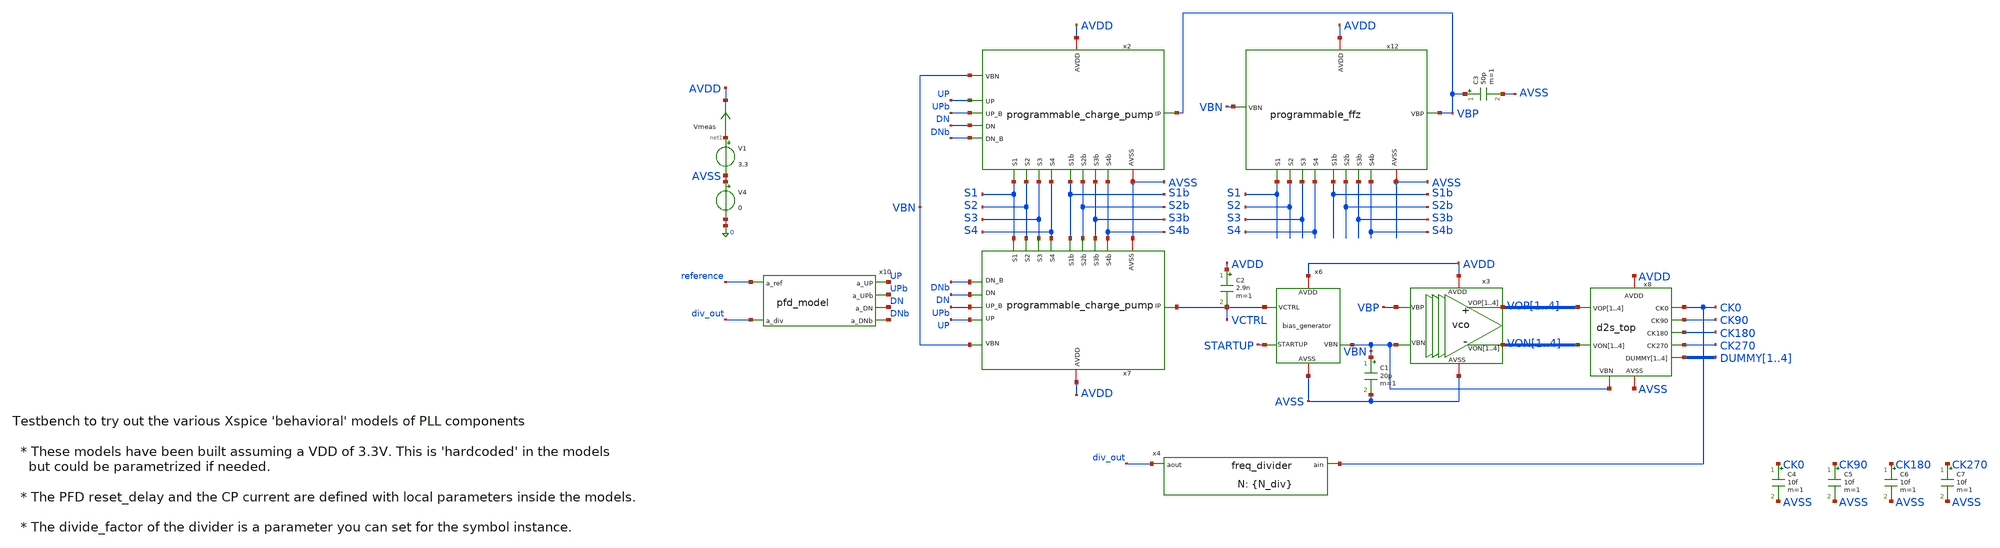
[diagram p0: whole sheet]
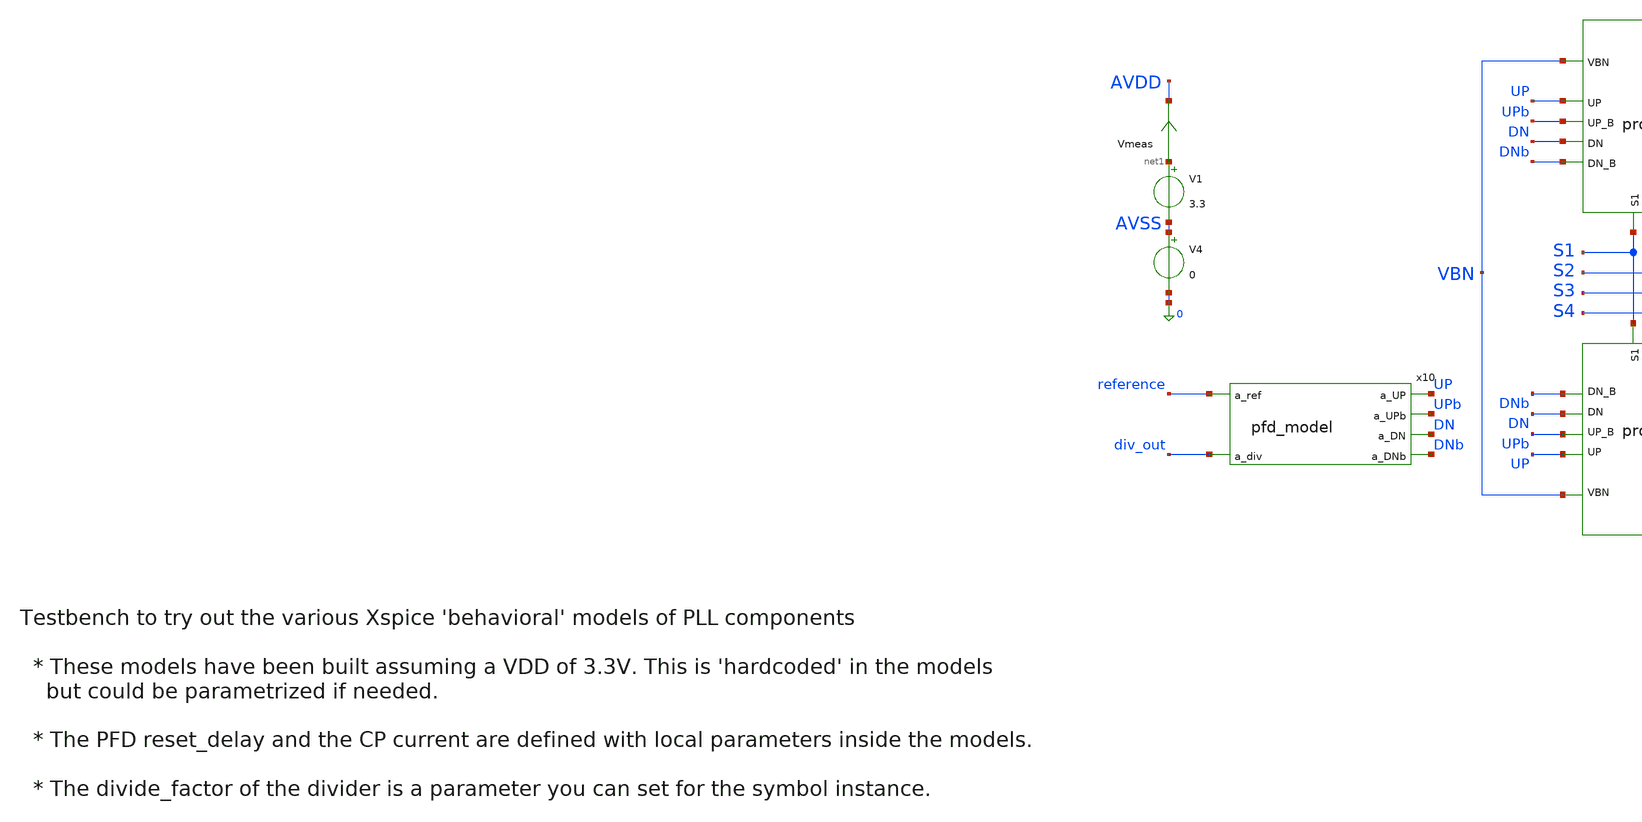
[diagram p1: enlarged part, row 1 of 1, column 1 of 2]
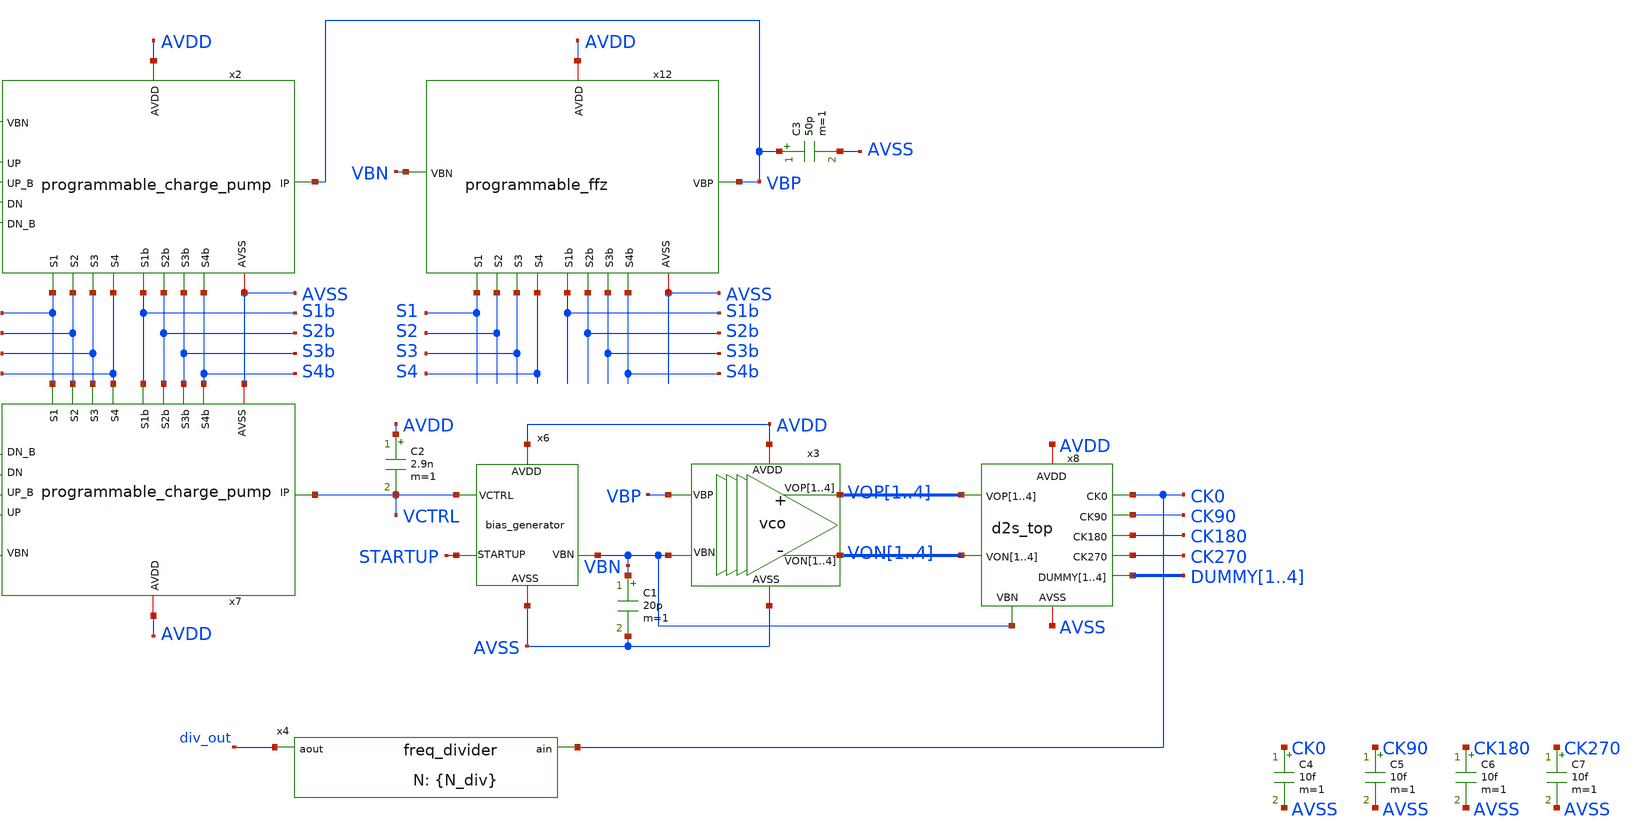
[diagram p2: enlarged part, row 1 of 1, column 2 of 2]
** sch_path: designs/libs/tb_pll/tb_PLL_CP_VCO_model.sch
**.subckt tb_PLL_CP_VCO_model
x4 div_out CK0 freq_divider divide_factor={N_div}
x3 VOP1 VOP2 VOP3 VOP4 VON1 VON2 VON3 VON4 AVDD AVSS VBP VBN vco
x6 VCTRL AVDD STARTUP AVSS VBN bias_generator
C2 AVDD VCTRL 2.9n m=1
V1 net1 AVSS 3.3
V4 AVSS 0 0
x2 AVSS AVDD UP UPb DN VBP DNb VBN S1b S1 S2b S2 S3b S3 S4b S4 programmable_charge_pump
x7 AVSS AVDD UP UPb DN VCTRL DNb VBN S1b S1 S2b S2 S3b S3 S4b S4 programmable_charge_pump
C1 VBN AVSS 20p m=1
C3 VBP AVSS 50p m=1
x12 VBP AVSS AVDD VBN S1b S1 S2b S2 S3b S3 S4b S4 programmable_ffz
x8 VOP1 VOP2 VOP3 VOP4 VON1 VON2 VON3 VON4 VBN DUMMY1 DUMMY2 DUMMY3 DUMMY4 CK0 CK90 CK180 CK270 AVDD
+ AVSS d2s_top
C4 CK0 AVSS 10f m=1
C5 CK90 AVSS 10f m=1
C6 CK180 AVSS 10f m=1
C7 CK270 AVSS 10f m=1
x10 reference UP UPb DN div_out DNb pfd_model
Vmeas net1 AVDD 0
.save i(vmeas)
**** begin user architecture code

.include $::180MCU_MODELS/design.ngspice
.lib $::180MCU_MODELS/sm141064.ngspice typical
*.lib $::180MCU_MODELS/sm141064.ngspice SS
*.lib $::180MCU_MODELS/sm141064.ngspice FF
*.lib $::180MCU_MODELS/sm141064.ngspice SF
*.lib $::180MCU_MODELS/sm141064.ngspice FS



==============Fref, N======================
.param f_ref=10MEG N_div=30

.param d1=0 d2=3.3 d3=3.3 d4=3.3
.param d1b=3.3 d2b=0 d3b=0 d4b=0

.ic v(VCTRL)=1 v(vbp)=1
==============Frequency Calculation========
.param tp_ref='td_ref/2' td_ref='1/f_ref'
Vref reference gnd pulse(0 3.3 0 500p 500p tp_ref td_ref)

.ic v(vop1)=3.3 v(von1)=0 v(startup)=0
.options reltol=1e-5 cshunt=1e-15
.options method=gear

VS1 S1 0 d1
VS2 S2 0 d2
VS3 S3 0 d3
VS4 S4 0 d4

VS1b S1b 0 d1b
VS2b S2b 0 d2b
VS3b S3b 0 d3b
VS4b S4b 0 d4b

.control
set wr_singlescale
set wr_vecnames

save v(VCTRL) v(vbp) v(vbn) v(reference) v(div_out) v(pre_div) v(CK0) v(CK90) v(CK180) v(CK270)
+ v(up) v(dn)

tran 10p 180u

linearize v(CK0) v(CK90) v(CK180) v(CK270) v(VCTRL) v(up) v(dn) v(vbp) v(vbn) v(reference)
+ v(div_out) v(pre_div) i(vmeas)

remzerovec

write tb5_3.raw
wrdata /foss/designs/synchronos-chipathon-2026/designs/libs/scripts/sim_data/tb5_3.txt tran.all
destroy all
.endc


**** end user architecture code
**.ends

* expanding   symbol:  libs/model_pll/freq_divider.sym # of pins=2
** sym_path: libs/model_pll/freq_divider.sym
** sch_path: libs/model_pll/freq_divider.sch
.subckt freq_divider aout ain  divide_factor=20
*.ipin ain
*.opin aout
* noconn ain
* noconn aout
**** begin user architecture code


* Behavioral Frequency Divider with robust Mixed-Signal Bridges

* Top-level parameter (Defaults to 10 if not passed by symbol)
.param divide_factor = 10

* MATH FIX: Guarantees at least 1 high cycle, targets 50% duty cycle
.param high_cycles = {max(1, floor(divide_factor/2))}

* Xspice digital frequency divider
adiv din dout divider
.model divider d_fdiv(div_factor = {divide_factor}  high_cycles = {high_cycles}  i_count = 0  rise_delay
+ = 100p fall_delay = 100p )
*+ rise_delay = 500p fall_delay = 500p )

* WINDOW FIX: Widened analog-to-digital thresholds to catch fast sine waves
aADC [ ain ] [ din ] adc_buff
.model adc_buff adc_bridge(in_low = 1.2 in_high = 2.1 rise_delay = 10p fall_delay = 10p)

* Digital-to-analog bridge
aDAC [ dout ] [ aout ] dac_buff
.model dac_buff dac_bridge(out_low = 0 out_high = 3.3 t_rise = 500p t_fall = 500p)


**** end user architecture code
.ends


* expanding   symbol:  libs/core_analog/vco/vco.sym # of pins=6
** sym_path: designs/libs/core_analog/vco/vco.sym
** sch_path: designs/libs/core_analog/vco/vco.sch
.subckt vco VOP1 VOP2 VOP3 VOP4 VON1 VON2 VON3 VON4 AVDD AVSS VBP VBN
*.opin VOP1,VOP2,VOP3,VOP4
*.opin VON1,VON2,VON3,VON4
*.ipin VBP
*.ipin VBN
*.iopin AVDD
*.iopin AVSS
x1 VOP1 AVDD VOP4 VON4 VON1 AVSS VBP VBN delay_stage
x2 VOP2 AVDD VON1 VOP1 VON2 AVSS VBP VBN delay_stage
x3 VOP3 AVDD VON2 VOP2 VON3 AVSS VBP VBN delay_stage
x4 VOP4 AVDD VON3 VOP3 VON4 AVSS VBP VBN delay_stage
.ends


* expanding   symbol:  libs/core_analog/bias_generator/bias_generator.sym # of pins=5
** sym_path: designs/libs/core_analog/bias_generator/bias_generator.sym
** sch_path: designs/libs/core_analog/bias_generator/bias_generator.sch
.subckt bias_generator VCTRL AVDD STARTUP AVSS VBN
*.ipin VCTRL
*.ipin STARTUP
*.iopin AVDD
*.iopin AVSS
*.opin VBN
x1 VBN AVDD net2 VCTRL AVSS net1 ota_5t
XM1 net1 net1 AVDD AVDD pfet_03v3 L=0.5u W=16.8u nf=1 ad='int((nf+1)/2) * W/nf * 0.18u' as='int((nf+2)/2) * W/nf * 0.18u'
+ pd='2*int((nf+1)/2) * (W/nf + 0.18u)' ps='2*int((nf+2)/2) * (W/nf + 0.18u)' nrd='0.18u / W' nrs='0.18u / W'
+ sa=0 sb=0 sd=0 m=16
XM8 net2 AVDD net4 AVSS nfet_03v3 L=0.5u W=2.08u nf=1 ad='int((nf+1)/2) * W/nf * 0.18u' as='int((nf+2)/2) * W/nf * 0.18u'
+ pd='2*int((nf+1)/2) * (W/nf + 0.18u)' ps='2*int((nf+2)/2) * (W/nf + 0.18u)' nrd='0.18u / W' nrs='0.18u / W'
+ sa=0 sb=0 sd=0 m=8
XM11 net1 AVDD net3 AVSS nfet_03v3 L=0.5u W=2.08u nf=1 ad='int((nf+1)/2) * W/nf * 0.18u' as='int((nf+2)/2) * W/nf * 0.18u'
+ pd='2*int((nf+1)/2) * (W/nf + 0.18u)' ps='2*int((nf+2)/2) * (W/nf + 0.18u)' nrd='0.18u / W' nrs='0.18u / W'
+ sa=0 sb=0 sd=0 m=8
XM2 net2 VCTRL AVDD AVDD pfet_03v3 L=1.5u W=1.1u nf=1 ad='int((nf+1)/2) * W/nf * 0.18u' as='int((nf+2)/2) * W/nf * 0.18u'
+ pd='2*int((nf+1)/2) * (W/nf + 0.18u)' ps='2*int((nf+2)/2) * (W/nf + 0.18u)' nrd='0.18u / W' nrs='0.18u / W'
+ sa=0 sb=0 sd=0 m=8
XM5 net2 net2 AVDD AVDD pfet_03v3 L=1.5u W=1.1u nf=1 ad='int((nf+1)/2) * W/nf * 0.18u' as='int((nf+2)/2) * W/nf * 0.18u'
+ pd='2*int((nf+1)/2) * (W/nf + 0.18u)' ps='2*int((nf+2)/2) * (W/nf + 0.18u)' nrd='0.18u / W' nrs='0.18u / W'
+ sa=0 sb=0 sd=0 m=8
XM7 net4 VBN AVSS AVSS nfet_03v3 L=0.5u W=11.25u nf=1 ad='int((nf+1)/2) * W/nf * 0.18u' as='int((nf+2)/2) * W/nf * 0.18u'
+ pd='2*int((nf+1)/2) * (W/nf + 0.18u)' ps='2*int((nf+2)/2) * (W/nf + 0.18u)' nrd='0.18u / W' nrs='0.18u / W'
+ sa=0 sb=0 sd=0 m=8
XM3 net3 VBN AVSS AVSS nfet_03v3 L=0.5u W=11.25u nf=1 ad='int((nf+1)/2) * W/nf * 0.18u' as='int((nf+2)/2) * W/nf * 0.18u'
+ pd='2*int((nf+1)/2) * (W/nf + 0.18u)' ps='2*int((nf+2)/2) * (W/nf + 0.18u)' nrd='0.18u / W' nrs='0.18u / W'
+ sa=0 sb=0 sd=0 m=8
XM4 net3 STARTUP AVSS AVSS nfet_03v3 L=0.5u W=11.25u nf=1 ad='int((nf+1)/2) * W/nf * 0.18u' as='int((nf+2)/2) * W/nf * 0.18u'
+ pd='2*int((nf+1)/2) * (W/nf + 0.18u)' ps='2*int((nf+2)/2) * (W/nf + 0.18u)' nrd='0.18u / W' nrs='0.18u / W'
+ sa=0 sb=0 sd=0 m=2
.ends


* expanding   symbol:  libs/core_analog/programmable_charge_pump/programmable_charge_pump.sym # of
*+ pins=16
** sym_path: designs/libs/core_analog/programmable_charge_pump/programmable_charge_pump.sym
** sch_path: designs/libs/core_analog/programmable_charge_pump/programmable_charge_pump.sch
.subckt programmable_charge_pump AVSS AVDD UP UP_B DN IP DN_B VBN S1b S1 S2b S2 S3b S3 S4b S4
*.ipin VBN
*.ipin S1b
*.ipin S1
*.ipin S2b
*.ipin S2
*.ipin S3b
*.ipin S3
*.ipin S4b
*.ipin S4
*.iopin AVSS
*.iopin AVDD
*.ipin UP
*.ipin UP_B
*.ipin DN
*.ipin DN_B
*.opin IP
x1 AVDD AVSS UP UP_B DN DN_B VBN1 IP S1b charge_pump
x61 AVDD AVSS UP UP_B DN DN_B VBN2 IP S2b charge_pump
x62 AVDD AVSS UP UP_B DN DN_B VBN2 IP S2b charge_pump
x71 AVDD AVSS UP UP_B DN DN_B VBN3 IP S3b charge_pump
x72 AVDD AVSS UP UP_B DN DN_B VBN3 IP S3b charge_pump
x73 AVDD AVSS UP UP_B DN DN_B VBN3 IP S3b charge_pump
x74 AVDD AVSS UP UP_B DN DN_B VBN3 IP S3b charge_pump
x81 AVDD AVSS UP UP_B DN DN_B VBN4 IP S4b charge_pump
x82 AVDD AVSS UP UP_B DN DN_B VBN4 IP S4b charge_pump
x83 AVDD AVSS UP UP_B DN DN_B VBN4 IP S4b charge_pump
x84 AVDD AVSS UP UP_B DN DN_B VBN4 IP S4b charge_pump
x85 AVDD AVSS UP UP_B DN DN_B VBN4 IP S4b charge_pump
x86 AVDD AVSS UP UP_B DN DN_B VBN4 IP S4b charge_pump
x87 AVDD AVSS UP UP_B DN DN_B VBN4 IP S4b charge_pump
x88 AVDD AVSS UP UP_B DN DN_B VBN4 IP S4b charge_pump
x2 VBN AVSS S1 VBN1 S1b AVDD transmission_gate
x0 AVDD AVSS UP UP_B DN DN_B VBN IP AVSS charge_pump
x3 VBN AVSS S2 VBN2 S2b AVDD transmission_gate
x4 VBN AVSS S3 VBN3 S3b AVDD transmission_gate
x5 VBN AVSS S4 VBN4 S4b AVDD transmission_gate
.ends


* expanding   symbol:  libs/core_analog/programmable_ffz/programmable_ffz.sym # of pins=12
** sym_path: designs/libs/core_analog/programmable_ffz/programmable_ffz.sym
** sch_path: designs/libs/core_analog/programmable_ffz/programmable_ffz.sch
.subckt programmable_ffz VBP AVSS AVDD VBN S1b S1 S2b S2 S3b S3 S4b S4
*.ipin VBN
*.ipin S1b
*.ipin S1
*.ipin S2b
*.ipin S2
*.ipin S3b
*.ipin S3
*.ipin S4b
*.ipin S4
*.iopin AVSS
*.iopin AVDD
*.opin VBP
x2 VBN AVSS S1 VBN1 S1b AVDD transmission_gate
x3 VBN AVSS S2 VBN2 S2b AVDD transmission_gate
x4 VBN AVSS S3 VBN3 S3b AVDD transmission_gate
x5 VBN AVSS S4 VBN4 S4b AVDD transmission_gate
x1 AVDD VBP VBN AVSS AVSS feed_forward_zero
x6 AVDD net1 VBN1 S1b AVSS feed_forward_zero
x71 AVDD net2[1] VBN2 S2b AVSS feed_forward_zero
x72 AVDD net2[0] VBN2 S2b AVSS feed_forward_zero
x11 AVDD net3[3] VBN3 S3b AVSS feed_forward_zero
x12 AVDD net3[2] VBN3 S3b AVSS feed_forward_zero
x13 AVDD net3[1] VBN3 S3b AVSS feed_forward_zero
x14 AVDD net3[0] VBN3 S3b AVSS feed_forward_zero
x21 AVDD net4[7] VBN4 S4b AVSS feed_forward_zero
x22 AVDD net4[6] VBN4 S4b AVSS feed_forward_zero
x23 AVDD net4[5] VBN4 S4b AVSS feed_forward_zero
x24 AVDD net4[4] VBN4 S4b AVSS feed_forward_zero
x25 AVDD net4[3] VBN4 S4b AVSS feed_forward_zero
x26 AVDD net4[2] VBN4 S4b AVSS feed_forward_zero
x27 AVDD net4[1] VBN4 S4b AVSS feed_forward_zero
x28 AVDD net4[0] VBN4 S4b AVSS feed_forward_zero
x7 net1 AVSS S1 VBP S1b AVDD transmission_gate
x81 net2[1] AVSS S2 VBP S2b AVDD transmission_gate
x82 net2[0] AVSS S2 VBP S2b AVDD transmission_gate
x91 net3[3] AVSS S3 VBP S3b AVDD transmission_gate
x92 net3[2] AVSS S3 VBP S3b AVDD transmission_gate
x93 net3[1] AVSS S3 VBP S3b AVDD transmission_gate
x94 net3[0] AVSS S3 VBP S3b AVDD transmission_gate
x101 net4[7] AVSS S4 VBP S4b AVDD transmission_gate
x102 net4[6] AVSS S4 VBP S4b AVDD transmission_gate
x103 net4[5] AVSS S4 VBP S4b AVDD transmission_gate
x104 net4[4] AVSS S4 VBP S4b AVDD transmission_gate
x105 net4[3] AVSS S4 VBP S4b AVDD transmission_gate
x106 net4[2] AVSS S4 VBP S4b AVDD transmission_gate
x107 net4[1] AVSS S4 VBP S4b AVDD transmission_gate
x108 net4[0] AVSS S4 VBP S4b AVDD transmission_gate
.ends


* expanding   symbol:  libs/core_analog/d2s_top/d2s_top.sym # of pins=10
** sym_path: designs/libs/core_analog/d2s_top/d2s_top.sym
** sch_path: designs/libs/core_analog/d2s_top/d2s_top.sch
.subckt d2s_top VOP1 VOP2 VOP3 VOP4 VON1 VON2 VON3 VON4 VBN DUMMY1 DUMMY2 DUMMY3 DUMMY4 CK0 CK90
+ CK180 CK270 AVDD AVSS
*.ipin VOP1,VOP2,VOP3,VOP4
*.ipin VON1,VON2,VON3,VON4
*.ipin VBN
*.opin DUMMY1,DUMMY2,DUMMY3,DUMMY4
*.opin CK0
*.opin CK90
*.opin CK180
*.opin CK270
*.iopin AVDD
*.iopin AVSS
x1 AVDD AVSS VON1 VOP1 VBN net8 d2s_converter
x2 AVDD AVSS VON3 VOP3 VBN net1 d2s_converter
x9 AVDD net8 CK0 AVSS inv
x10 AVDD net1 CK90 AVSS inv
x3 AVDD AVSS VOP1 VON1 VBN net2 d2s_converter
x4 AVDD net2 CK180 AVSS inv
x5 AVDD AVSS VOP3 VON3 VBN net3 d2s_converter
x6 AVDD net3 CK270 AVSS inv
x7 AVDD AVSS VON2 VOP2 VBN net7 d2s_converter
x8 AVDD AVSS VON4 VOP4 VBN net4 d2s_converter
x11 AVDD net7 DUMMY1 AVSS inv
x12 AVDD net4 DUMMY2 AVSS inv
x13 AVDD AVSS VOP2 VON2 VBN net5 d2s_converter
x14 AVDD net5 DUMMY3 AVSS inv
x15 AVDD AVSS VOP4 VON4 VBN net6 d2s_converter
x16 AVDD net6 DUMMY4 AVSS inv
.ends


* expanding   symbol:  libs/model_pll/pfd_model.sym # of pins=6
** sym_path: designs/libs/model_pll/pfd_model.sym
** sch_path: designs/libs/model_pll/pfd_model.sch
.subckt pfd_model a_ref a_UP a_UPb a_DN a_div a_DNb
*.ipin a_ref
*.ipin a_div
*.opin a_UP
*.opin a_UPb
*.opin a_DN
*.opin a_DNb
* noconn a_ref
* noconn a_div
* noconn a_UP
* noconn a_UPb
* noconn a_DN
* noconn a_DNb
**** begin user architecture code


* PFD Model using digital Xspice components

* pfd_delay local parameter sets the duration of the overlap (dead-band elimination)
* Reduced from 10ns to 200ps to prevent massive Vctrl ripple
*.param pfd_delay = 200p
.param pfd_delay = 2n
*.param pfd_delay = 10n

** Digital 1 and 0 to drive Flip-Flops
aone 0 d_d1 d_inv
azero d_d1 d_d0 d_inv
.model d_inv d_inverter()

** Flip Flops
ad1 d_d1 d_R d_d0 d_rset d_U d_U_ flop1
ad2 d_d1 d_V d_d0 d_rset d_D d_D_ flop1
.model flop1 d_dff(clk_delay = 1.0e-10 set_delay = 1.0e-10  reset_delay = {pfd_delay} ic = 2 rise_delay
+ = 1.0e-10  fall_delay = 1e-10)

* AND Gate
aa1 [d_U d_D] d_rset and1
.model and1 d_and(rise_delay = 1e-10 fall_delay = 1e-10   input_load = 0.5e-12)

* WINDOW FIX: Widened thresholds to catch fast analog edges safely
aADC [ a_ref a_div ] [ d_R d_V ] adc_buff
.model adc_buff adc_bridge(in_low = 1.2 in_high = 2.1 rise_delay = 10p fall_delay = 10p)

* DAC FIX: Explicitly defined analog rise/fall times to prevent solver crashes
aDAC [ d_U d_U_ d_D d_D_ d_rset d_R d_V d_d1 d_d0 ] [ a_UP a_UPb a_DN a_DNb a_rset a_R a_V a_d1
+ a_d0] dac_buff
.model dac_buff dac_bridge(out_low = 0 out_high = 3.3 t_rise = 500p t_fall = 500p)
*.model dac_buff dac_bridge(out_low = 0 out_high = 3.3 t_rise = 1u t_fall = 1u)


**** end user architecture code
.ends


* expanding   symbol:  libs/core_analog/delay_stage/delay_stage.sym # of pins=8
** sym_path: designs/libs/core_analog/delay_stage/delay_stage.sym
** sch_path: designs/libs/core_analog/delay_stage/delay_stage.sch
.subckt delay_stage VOP AVDD VIP VIN VON AVSS VBP VBN
*.ipin VIP
*.ipin VIN
*.opin VOP
*.opin VON
*.iopin AVDD
*.iopin AVSS
*.ipin VBP
*.ipin VBN
XM5 VON VIP net1 AVSS nfet_03v3 L=0.5u W=2.08u nf=1 ad='int((nf+1)/2) * W/nf * 0.18u' as='int((nf+2)/2) * W/nf * 0.18u'
+ pd='2*int((nf+1)/2) * (W/nf + 0.18u)' ps='2*int((nf+2)/2) * (W/nf + 0.18u)' nrd='0.18u / W' nrs='0.18u / W'
+ sa=0 sb=0 sd=0 m=8
XM2 VON VON AVDD AVDD pfet_03v3 L=1.5u W=1.1u nf=1 ad='int((nf+1)/2) * W/nf * 0.18u' as='int((nf+2)/2) * W/nf * 0.18u'
+ pd='2*int((nf+1)/2) * (W/nf + 0.18u)' ps='2*int((nf+2)/2) * (W/nf + 0.18u)' nrd='0.18u / W' nrs='0.18u / W'
+ sa=0 sb=0 sd=0 m=8
XM6 VOP VIN net1 AVSS nfet_03v3 L=0.5u W=2.08u nf=1 ad='int((nf+1)/2) * W/nf * 0.18u' as='int((nf+2)/2) * W/nf * 0.18u'
+ pd='2*int((nf+1)/2) * (W/nf + 0.18u)' ps='2*int((nf+2)/2) * (W/nf + 0.18u)' nrd='0.18u / W' nrs='0.18u / W'
+ sa=0 sb=0 sd=0 m=8
XM1 VON VBP AVDD AVDD pfet_03v3 L=1.5u W=1.1u nf=1 ad='int((nf+1)/2) * W/nf * 0.18u' as='int((nf+2)/2) * W/nf * 0.18u'
+ pd='2*int((nf+1)/2) * (W/nf + 0.18u)' ps='2*int((nf+2)/2) * (W/nf + 0.18u)' nrd='0.18u / W' nrs='0.18u / W'
+ sa=0 sb=0 sd=0 m=8
XM3 VOP VBP AVDD AVDD pfet_03v3 L=1.5u W=1.1u nf=1 ad='int((nf+1)/2) * W/nf * 0.18u' as='int((nf+2)/2) * W/nf * 0.18u'
+ pd='2*int((nf+1)/2) * (W/nf + 0.18u)' ps='2*int((nf+2)/2) * (W/nf + 0.18u)' nrd='0.18u / W' nrs='0.18u / W'
+ sa=0 sb=0 sd=0 m=8
XM4 VOP VOP AVDD AVDD pfet_03v3 L=1.5u W=1.1u nf=1 ad='int((nf+1)/2) * W/nf * 0.18u' as='int((nf+2)/2) * W/nf * 0.18u'
+ pd='2*int((nf+1)/2) * (W/nf + 0.18u)' ps='2*int((nf+2)/2) * (W/nf + 0.18u)' nrd='0.18u / W' nrs='0.18u / W'
+ sa=0 sb=0 sd=0 m=8
XM8 net1 VBN AVSS AVSS nfet_03v3 L=0.5u W=11.25u nf=1 ad='int((nf+1)/2) * W/nf * 0.18u' as='int((nf+2)/2) * W/nf * 0.18u'
+ pd='2*int((nf+1)/2) * (W/nf + 0.18u)' ps='2*int((nf+2)/2) * (W/nf + 0.18u)' nrd='0.18u / W' nrs='0.18u / W'
+ sa=0 sb=0 sd=0 m=8
.ends


* expanding   symbol:  libs/core_analog/ota_5t/ota_5t.sym # of pins=6
** sym_path: designs/libs/core_analog/ota_5t/ota_5t.sym
** sch_path: designs/libs/core_analog/ota_5t/ota_5t.sch
.subckt ota_5t VO AVDD VI+ VI- AVSS VB
*.ipin VI+
*.ipin VI-
*.ipin VB
*.iopin AVDD
*.iopin AVSS
*.opin VO
XM1 VO VI- net2 AVDD pfet_03v3 L=0.5u W=6.55u nf=1 ad='int((nf+1)/2) * W/nf * 0.18u' as='int((nf+2)/2) * W/nf * 0.18u'
+ pd='2*int((nf+1)/2) * (W/nf + 0.18u)' ps='2*int((nf+2)/2) * (W/nf + 0.18u)' nrd='0.18u / W' nrs='0.18u / W'
+ sa=0 sb=0 sd=0 m=8
XM4 VO net1 AVSS AVSS nfet_03v3 L=0.5u W=4.8u nf=1 ad='int((nf+1)/2) * W/nf * 0.18u' as='int((nf+2)/2) * W/nf * 0.18u'
+ pd='2*int((nf+1)/2) * (W/nf + 0.18u)' ps='2*int((nf+2)/2) * (W/nf + 0.18u)' nrd='0.18u / W' nrs='0.18u / W'
+ sa=0 sb=0 sd=0 m=4
XM3 net2 VB net3 AVDD pfet_03v3 L=0.5u W=8.3u nf=1 ad='int((nf+1)/2) * W/nf * 0.18u' as='int((nf+2)/2) * W/nf * 0.18u'
+ pd='2*int((nf+1)/2) * (W/nf + 0.18u)' ps='2*int((nf+2)/2) * (W/nf + 0.18u)' nrd='0.18u / W' nrs='0.18u / W'
+ sa=0 sb=0 sd=0 m=16
XM2 net1 VI+ net2 AVDD pfet_03v3 L=0.5u W=6.55u nf=1 ad='int((nf+1)/2) * W/nf * 0.18u' as='int((nf+2)/2) * W/nf * 0.18u'
+ pd='2*int((nf+1)/2) * (W/nf + 0.18u)' ps='2*int((nf+2)/2) * (W/nf + 0.18u)' nrd='0.18u / W' nrs='0.18u / W'
+ sa=0 sb=0 sd=0 m=8
XM5 net1 net1 AVSS AVSS nfet_03v3 L=0.5u W=4.8u nf=1 ad='int((nf+1)/2) * W/nf * 0.18u' as='int((nf+2)/2) * W/nf * 0.18u'
+ pd='2*int((nf+1)/2) * (W/nf + 0.18u)' ps='2*int((nf+2)/2) * (W/nf + 0.18u)' nrd='0.18u / W' nrs='0.18u / W'
+ sa=0 sb=0 sd=0 m=4
Vmeas AVDD net3 0
.save i(vmeas)
.ends


* expanding   symbol:  libs/core_analog/charge_pump/charge_pump.sym # of pins=9
** sym_path: designs/libs/core_analog/charge_pump/charge_pump.sym
** sch_path: designs/libs/core_analog/charge_pump/charge_pump.sch
.subckt charge_pump VDD VSS UP UP_B DN DN_B VBN IP S
*.iopin VDD
*.iopin VSS
*.ipin UP
*.ipin UP_B
*.ipin DN
*.ipin DN_B
*.ipin VBN
*.iopin IP
*.ipin S
x1 net5 net5 VDD net5 VDD cp_sym_load
x2 net3 net3 VDD net3 VDD cp_sym_load
x3 net4 net4 VDD net4 VDD cp_sym_load
x4 net5 net5 VDD IP VDD cp_sym_load
XM1 net1 VBN VSS VSS nfet_03v3 L=0.5u W=11.25u nf=1 ad='int((nf+1)/2) * W/nf * 0.18u' as='int((nf+2)/2) * W/nf * 0.18u'
+ pd='2*int((nf+1)/2) * (W/nf + 0.18u)' ps='2*int((nf+2)/2) * (W/nf + 0.18u)' nrd='0.18u / W' nrs='0.18u / W'
+ sa=0 sb=0 sd=0 m=1
XM3 net5 DN net1 VSS nfet_03v3 L=0.5u W=2.08u nf=1 ad='int((nf+1)/2) * W/nf * 0.18u' as='int((nf+2)/2) * W/nf * 0.18u'
+ pd='2*int((nf+1)/2) * (W/nf + 0.18u)' ps='2*int((nf+2)/2) * (W/nf + 0.18u)' nrd='0.18u / W' nrs='0.18u / W'
+ sa=0 sb=0 sd=0 m=1
XM7 VBN S VSS VSS nfet_03v3 L=0.5u W=1u nf=1 ad='int((nf+1)/2) * W/nf * 0.18u' as='int((nf+2)/2) * W/nf * 0.18u'
+ pd='2*int((nf+1)/2) * (W/nf + 0.18u)' ps='2*int((nf+2)/2) * (W/nf + 0.18u)' nrd='0.18u / W' nrs='0.18u / W'
+ sa=0 sb=0 sd=0 m=1
XM8 VBN S VSS VSS nfet_03v3 L=0.5u W=1u nf=1 ad='int((nf+1)/2) * W/nf * 0.18u' as='int((nf+2)/2) * W/nf * 0.18u'
+ pd='2*int((nf+1)/2) * (W/nf + 0.18u)' ps='2*int((nf+2)/2) * (W/nf + 0.18u)' nrd='0.18u / W' nrs='0.18u / W'
+ sa=0 sb=0 sd=0 m=1
XM4 net3 DN_B net1 VSS nfet_03v3 L=0.5u W=2.08u nf=1 ad='int((nf+1)/2) * W/nf * 0.18u' as='int((nf+2)/2) * W/nf * 0.18u'
+ pd='2*int((nf+1)/2) * (W/nf + 0.18u)' ps='2*int((nf+2)/2) * (W/nf + 0.18u)' nrd='0.18u / W' nrs='0.18u / W'
+ sa=0 sb=0 sd=0 m=1
XM5 net4 UP_B net2 VSS nfet_03v3 L=0.5u W=2.08u nf=1 ad='int((nf+1)/2) * W/nf * 0.18u' as='int((nf+2)/2) * W/nf * 0.18u'
+ pd='2*int((nf+1)/2) * (W/nf + 0.18u)' ps='2*int((nf+2)/2) * (W/nf + 0.18u)' nrd='0.18u / W' nrs='0.18u / W'
+ sa=0 sb=0 sd=0 m=1
XM6 IP UP net2 VSS nfet_03v3 L=0.5u W=2.08u nf=1 ad='int((nf+1)/2) * W/nf * 0.18u' as='int((nf+2)/2) * W/nf * 0.18u'
+ pd='2*int((nf+1)/2) * (W/nf + 0.18u)' ps='2*int((nf+2)/2) * (W/nf + 0.18u)' nrd='0.18u / W' nrs='0.18u / W'
+ sa=0 sb=0 sd=0 m=1
XM2 net2 VBN VSS VSS nfet_03v3 L=0.5u W=11.25u nf=1 ad='int((nf+1)/2) * W/nf * 0.18u' as='int((nf+2)/2) * W/nf * 0.18u'
+ pd='2*int((nf+1)/2) * (W/nf + 0.18u)' ps='2*int((nf+2)/2) * (W/nf + 0.18u)' nrd='0.18u / W' nrs='0.18u / W'
+ sa=0 sb=0 sd=0 m=1
.ends


* expanding   symbol:  libs/core_analog/transmission_gate/transmission_gate.sym # of pins=6
** sym_path: designs/libs/core_analog/transmission_gate/transmission_gate.sym
** sch_path: designs/libs/core_analog/transmission_gate/transmission_gate.sch
.subckt transmission_gate ind vss clkn ins clkp vdd
*.iopin ind
*.iopin ins
*.iopin clkn
*.iopin clkp
*.iopin vdd
*.iopin vss
XM1 ind clkp ins vdd pfet_03v3 L=0.5u W=3.0u nf=1 ad='int((nf+1)/2) * W/nf * 0.18u' as='int((nf+2)/2) * W/nf * 0.18u'
+ pd='2*int((nf+1)/2) * (W/nf + 0.18u)' ps='2*int((nf+2)/2) * (W/nf + 0.18u)' nrd='0.18u / W' nrs='0.18u / W'
+ sa=0 sb=0 sd=0 m=1
XM2 ind clkn ins vss nfet_03v3 L=0.5u W=1.0u nf=1 ad='int((nf+1)/2) * W/nf * 0.18u' as='int((nf+2)/2) * W/nf * 0.18u'
+ pd='2*int((nf+1)/2) * (W/nf + 0.18u)' ps='2*int((nf+2)/2) * (W/nf + 0.18u)' nrd='0.18u / W' nrs='0.18u / W'
+ sa=0 sb=0 sd=0 m=1
.ends


* expanding   symbol:  libs/core_analog/feed_forward_zero/feed_forward_zero.sym # of pins=5
** sym_path: designs/libs/core_analog/feed_forward_zero/feed_forward_zero.sym
** sch_path: designs/libs/core_analog/feed_forward_zero/feed_forward_zero.sch
.subckt feed_forward_zero AVDD VBP VBN S AVSS
*.opin VBP
*.iopin AVDD
*.iopin AVSS
*.ipin VBN
*.ipin S
XM1 VBP VBP AVDD AVDD pfet_03v3 L=1.5u W=1.1u nf=1 ad='int((nf+1)/2) * W/nf * 0.18u' as='int((nf+2)/2) * W/nf * 0.18u'
+ pd='2*int((nf+1)/2) * (W/nf + 0.18u)' ps='2*int((nf+2)/2) * (W/nf + 0.18u)' nrd='0.18u / W' nrs='0.18u / W'
+ sa=0 sb=0 sd=0 m=2
XM2 VBP VBP AVDD AVDD pfet_03v3 L=1.5u W=1.1u nf=1 ad='int((nf+1)/2) * W/nf * 0.18u' as='int((nf+2)/2) * W/nf * 0.18u'
+ pd='2*int((nf+1)/2) * (W/nf + 0.18u)' ps='2*int((nf+2)/2) * (W/nf + 0.18u)' nrd='0.18u / W' nrs='0.18u / W'
+ sa=0 sb=0 sd=0 m=2
XM3 VBP AVDD net1 AVSS nfet_03v3 L=0.5u W=2.08u nf=1 ad='int((nf+1)/2) * W/nf * 0.18u' as='int((nf+2)/2) * W/nf * 0.18u'
+ pd='2*int((nf+1)/2) * (W/nf + 0.18u)' ps='2*int((nf+2)/2) * (W/nf + 0.18u)' nrd='0.18u / W' nrs='0.18u / W'
+ sa=0 sb=0 sd=0 m=2
XM4 net1 VBN AVSS AVSS nfet_03v3 L=0.5u W=11.25u nf=1 ad='int((nf+1)/2) * W/nf * 0.18u' as='int((nf+2)/2) * W/nf * 0.18u'
+ pd='2*int((nf+1)/2) * (W/nf + 0.18u)' ps='2*int((nf+2)/2) * (W/nf + 0.18u)' nrd='0.18u / W' nrs='0.18u / W'
+ sa=0 sb=0 sd=0 m=2
XM7 VBN S AVSS AVSS nfet_03v3 L=0.5u W=1u nf=1 ad='int((nf+1)/2) * W/nf * 0.18u' as='int((nf+2)/2) * W/nf * 0.18u'
+ pd='2*int((nf+1)/2) * (W/nf + 0.18u)' ps='2*int((nf+2)/2) * (W/nf + 0.18u)' nrd='0.18u / W' nrs='0.18u / W'
+ sa=0 sb=0 sd=0 m=1
.ends


* expanding   symbol:  libs/core_analog/d2s_converter/d2s_converter.sym # of pins=6
** sym_path: designs/libs/core_analog/d2s_converter/d2s_converter.sym
** sch_path: designs/libs/core_analog/d2s_converter/d2s_converter.sch
.subckt d2s_converter AVDD AVSS VIN VIP VBN VO
*.iopin AVDD
*.iopin AVSS
*.ipin VIN
*.ipin VIP
*.opin VO
*.ipin VBN
XM2 VOPB VIN i1 AVSS nfet_03v3 L=0.3u W=1.9u nf=1 ad='int((nf+1)/2) * W/nf * 0.18u' as='int((nf+2)/2) * W/nf * 0.18u'
+ pd='2*int((nf+1)/2) * (W/nf + 0.18u)' ps='2*int((nf+2)/2) * (W/nf + 0.18u)' nrd='0.18u / W' nrs='0.18u / W'
+ sa=0 sb=0 sd=0 m=4
XM4 VOPB VOPB AVDD AVDD pfet_03v3 L=0.3u W=1.4u nf=1 ad='int((nf+1)/2) * W/nf * 0.18u' as='int((nf+2)/2) * W/nf * 0.18u'
+ pd='2*int((nf+1)/2) * (W/nf + 0.18u)' ps='2*int((nf+2)/2) * (W/nf + 0.18u)' nrd='0.18u / W' nrs='0.18u / W'
+ sa=0 sb=0 sd=0 m=4
XM11 VOB VOB AVSS AVSS nfet_03v3 L=0.3u W=1.5u nf=1 ad='int((nf+1)/2) * W/nf * 0.18u' as='int((nf+2)/2) * W/nf * 0.18u'
+ pd='2*int((nf+1)/2) * (W/nf + 0.18u)' ps='2*int((nf+2)/2) * (W/nf + 0.18u)' nrd='0.18u / W' nrs='0.18u / W'
+ sa=0 sb=0 sd=0 m=4
XM13 VOB VOP AVDD AVDD pfet_03v3 L=0.3u W=2u nf=1 ad='int((nf+1)/2) * W/nf * 0.18u' as='int((nf+2)/2) * W/nf * 0.18u'
+ pd='2*int((nf+1)/2) * (W/nf + 0.18u)' ps='2*int((nf+2)/2) * (W/nf + 0.18u)' nrd='0.18u / W' nrs='0.18u / W'
+ sa=0 sb=0 sd=0 m=4
XM3 VOP VIP i1 AVSS nfet_03v3 L=0.3u W=1.9u nf=1 ad='int((nf+1)/2) * W/nf * 0.18u' as='int((nf+2)/2) * W/nf * 0.18u'
+ pd='2*int((nf+1)/2) * (W/nf + 0.18u)' ps='2*int((nf+2)/2) * (W/nf + 0.18u)' nrd='0.18u / W' nrs='0.18u / W'
+ sa=0 sb=0 sd=0 m=4
XM5 VOP VOPB AVDD AVDD pfet_03v3 L=0.3u W=1.4u nf=1 ad='int((nf+1)/2) * W/nf * 0.18u' as='int((nf+2)/2) * W/nf * 0.18u'
+ pd='2*int((nf+1)/2) * (W/nf + 0.18u)' ps='2*int((nf+2)/2) * (W/nf + 0.18u)' nrd='0.18u / W' nrs='0.18u / W'
+ sa=0 sb=0 sd=0 m=4
XM7 VONB VIP i2 AVSS nfet_03v3 L=0.3u W=1.9u nf=1 ad='int((nf+1)/2) * W/nf * 0.18u' as='int((nf+2)/2) * W/nf * 0.18u'
+ pd='2*int((nf+1)/2) * (W/nf + 0.18u)' ps='2*int((nf+2)/2) * (W/nf + 0.18u)' nrd='0.18u / W' nrs='0.18u / W'
+ sa=0 sb=0 sd=0 m=4
XM8 VONB VONB AVDD AVDD pfet_03v3 L=0.3u W=1.4u nf=1 ad='int((nf+1)/2) * W/nf * 0.18u' as='int((nf+2)/2) * W/nf * 0.18u'
+ pd='2*int((nf+1)/2) * (W/nf + 0.18u)' ps='2*int((nf+2)/2) * (W/nf + 0.18u)' nrd='0.18u / W' nrs='0.18u / W'
+ sa=0 sb=0 sd=0 m=4
XM9 VON VIN i2 AVSS nfet_03v3 L=0.3u W=1.9u nf=1 ad='int((nf+1)/2) * W/nf * 0.18u' as='int((nf+2)/2) * W/nf * 0.18u'
+ pd='2*int((nf+1)/2) * (W/nf + 0.18u)' ps='2*int((nf+2)/2) * (W/nf + 0.18u)' nrd='0.18u / W' nrs='0.18u / W'
+ sa=0 sb=0 sd=0 m=4
XM10 VON VONB AVDD AVDD pfet_03v3 L=0.3u W=1.4u nf=1 ad='int((nf+1)/2) * W/nf * 0.18u' as='int((nf+2)/2) * W/nf * 0.18u'
+ pd='2*int((nf+1)/2) * (W/nf + 0.18u)' ps='2*int((nf+2)/2) * (W/nf + 0.18u)' nrd='0.18u / W' nrs='0.18u / W'
+ sa=0 sb=0 sd=0 m=4
XM14 VO VON AVDD AVDD pfet_03v3 L=0.3u W=2u nf=1 ad='int((nf+1)/2) * W/nf * 0.18u' as='int((nf+2)/2) * W/nf * 0.18u'
+ pd='2*int((nf+1)/2) * (W/nf + 0.18u)' ps='2*int((nf+2)/2) * (W/nf + 0.18u)' nrd='0.18u / W' nrs='0.18u / W'
+ sa=0 sb=0 sd=0 m=4
XM12 VO VOB AVSS AVSS nfet_03v3 L=0.3u W=1.5u nf=1 ad='int((nf+1)/2) * W/nf * 0.18u' as='int((nf+2)/2) * W/nf * 0.18u'
+ pd='2*int((nf+1)/2) * (W/nf + 0.18u)' ps='2*int((nf+2)/2) * (W/nf + 0.18u)' nrd='0.18u / W' nrs='0.18u / W'
+ sa=0 sb=0 sd=0 m=4
XM1 i1 VBN AVSS AVSS nfet_03v3 L=0.5u W=11.25u nf=1 ad='int((nf+1)/2) * W/nf * 0.18u' as='int((nf+2)/2) * W/nf * 0.18u'
+ pd='2*int((nf+1)/2) * (W/nf + 0.18u)' ps='2*int((nf+2)/2) * (W/nf + 0.18u)' nrd='0.18u / W' nrs='0.18u / W'
+ sa=0 sb=0 sd=0 m=4
XM6 i2 VBN AVSS AVSS nfet_03v3 L=0.5u W=11.25u nf=1 ad='int((nf+1)/2) * W/nf * 0.18u' as='int((nf+2)/2) * W/nf * 0.18u'
+ pd='2*int((nf+1)/2) * (W/nf + 0.18u)' ps='2*int((nf+2)/2) * (W/nf + 0.18u)' nrd='0.18u / W' nrs='0.18u / W'
+ sa=0 sb=0 sd=0 m=4
.ends


* expanding   symbol:  libs/core_analog/inv/inv.sym # of pins=4
** sym_path: designs/libs/core_analog/inv/inv.sym
** sch_path: designs/libs/core_analog/inv/inv.sch
.subckt inv AVDD IN OUT AVSS
*.ipin IN
*.iopin AVDD
*.iopin AVSS
*.opin OUT
XM1 OUT IN AVDD AVDD pfet_03v3 L=0.28u W=0.9u nf=1 ad='int((nf+1)/2) * W/nf * 0.18u' as='int((nf+2)/2) * W/nf * 0.18u'
+ pd='2*int((nf+1)/2) * (W/nf + 0.18u)' ps='2*int((nf+2)/2) * (W/nf + 0.18u)' nrd='0.18u / W' nrs='0.18u / W'
+ sa=0 sb=0 sd=0 m=1
XM2 OUT IN AVSS AVSS nfet_03v3 L=0.28u W=0.3u nf=1 ad='int((nf+1)/2) * W/nf * 0.18u' as='int((nf+2)/2) * W/nf * 0.18u'
+ pd='2*int((nf+1)/2) * (W/nf + 0.18u)' ps='2*int((nf+2)/2) * (W/nf + 0.18u)' nrd='0.18u / W' nrs='0.18u / W'
+ sa=0 sb=0 sd=0 m=1
.ends


* expanding   symbol:  libs/core_analog/cp_sym_load/cp_sym_load.sym # of pins=5
** sym_path: designs/libs/core_analog/cp_sym_load/cp_sym_load.sym
** sch_path: designs/libs/core_analog/cp_sym_load/cp_sym_load.sch
.subckt cp_sym_load G1 G2 S D VDD
*.ipin G1
*.ipin G2
*.iopin S
*.iopin D
*.iopin VDD
XM1 D G1 S VDD pfet_03v3 L=1.5u W=1.1u nf=1 ad='int((nf+1)/2) * W/nf * 0.18u' as='int((nf+2)/2) * W/nf * 0.18u'
+ pd='2*int((nf+1)/2) * (W/nf + 0.18u)' ps='2*int((nf+2)/2) * (W/nf + 0.18u)' nrd='0.18u / W' nrs='0.18u / W'
+ sa=0 sb=0 sd=0 m=1
XM2 D G2 S VDD pfet_03v3 L=1.5u W=1.1u nf=1 ad='int((nf+1)/2) * W/nf * 0.18u' as='int((nf+2)/2) * W/nf * 0.18u'
+ pd='2*int((nf+1)/2) * (W/nf + 0.18u)' ps='2*int((nf+2)/2) * (W/nf + 0.18u)' nrd='0.18u / W' nrs='0.18u / W'
+ sa=0 sb=0 sd=0 m=1
.ends

.end
